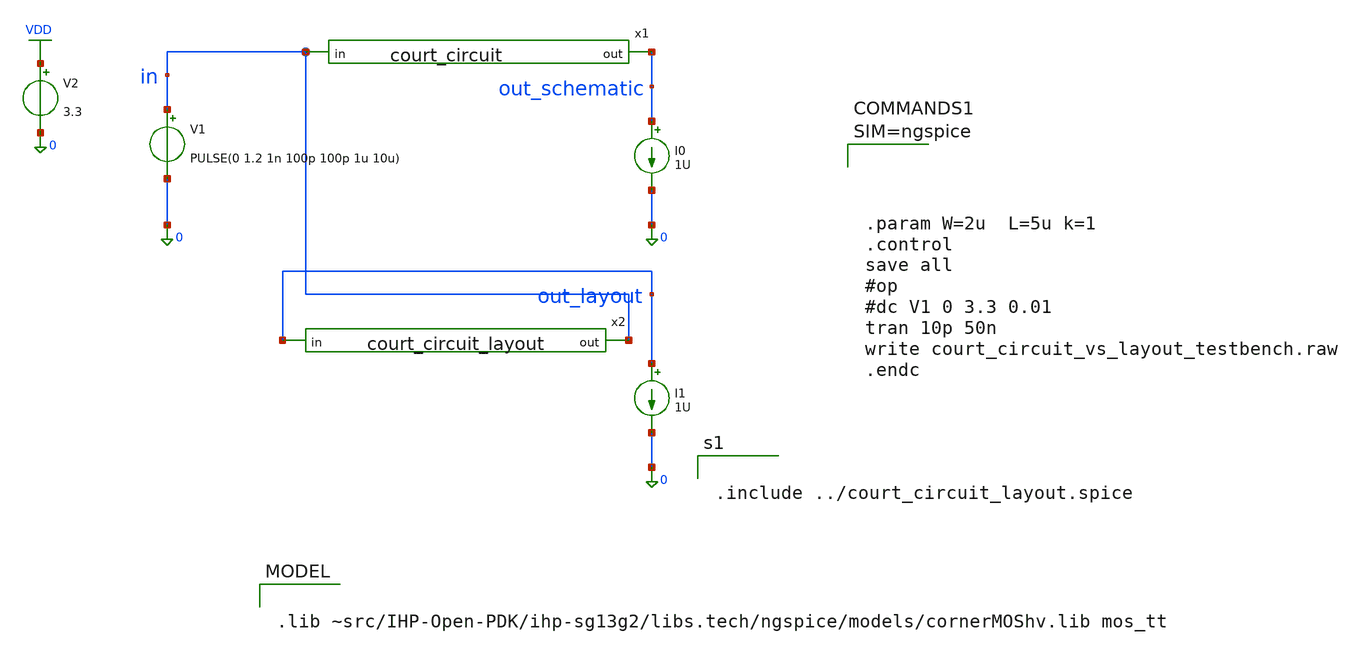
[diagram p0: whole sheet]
** sch_path: court_circuit_actif/court_circuit_vs_layout_testbench.sch
**.subckt court_circuit_vs_layout_testbench
x1 out_schematic in court_circuit
V1 in 0 PULSE(0 1.2 1n 100p 100p 1u 10u)
I0 out_schematic 0 1U
V2 VDD 0 3.3
I1 out_layout 0 1U
x2 in out_layout court_circuit_layout
**** begin user architecture code





.param W=2u  L=5u k=1
.control
save all
#op
#dc V1 0 3.3 0.01
tran 10p 50n
write court_circuit_vs_layout_testbench.raw
.endc




.lib ~src/IHP-Open-PDK/ihp-sg13g2/libs.tech/ngspice/models/cornerMOShv.lib mos_tt


.include ../court_circuit_layout.spice


**** end user architecture code
**.ends
.GLOBAL VDD
.end
